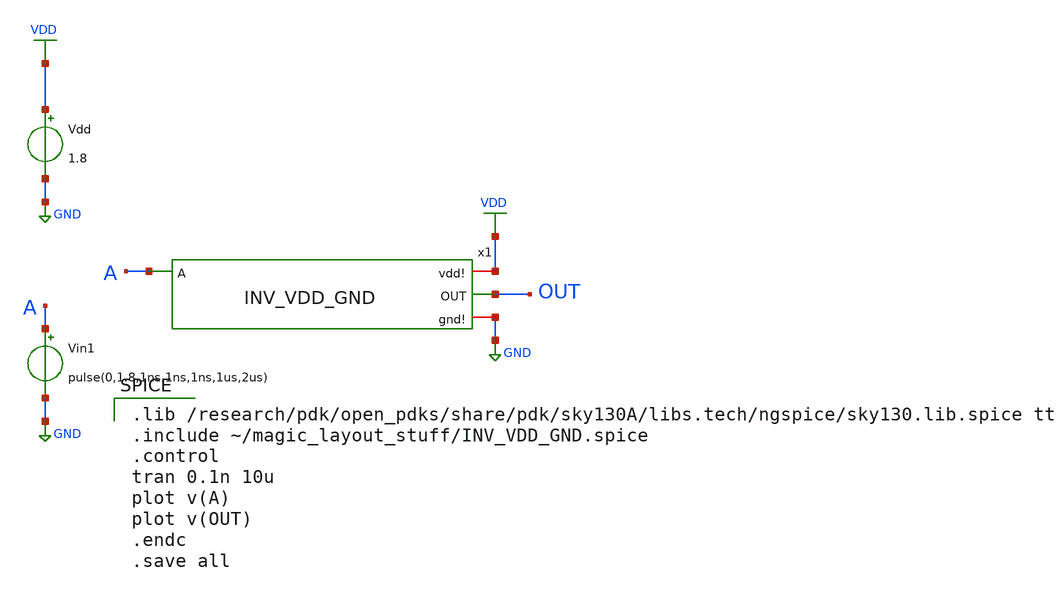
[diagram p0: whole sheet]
** sch_path: skywater_stuff/INV_VDD_GND_sim.sch
**.subckt INV_VDD_GND_sim
x1 A OUT VDD GND INV_VDD_GND
Vdd VDD GND 1.8
Vin1 A GND pulse(0,1.8,1ns,1ns,1ns,1us,2us)
**** begin user architecture code

.lib /research/pdk/open_pdks/share/pdk/sky130A/libs.tech/ngspice/sky130.lib.spice tt
.include ~/magic_layout_stuff/INV_VDD_GND.spice
.control
tran 0.1n 10u
plot v(A)
plot v(OUT)
.endc
.save all

**** end user architecture code
**.ends
.GLOBAL GND
.GLOBAL VDD
.end
